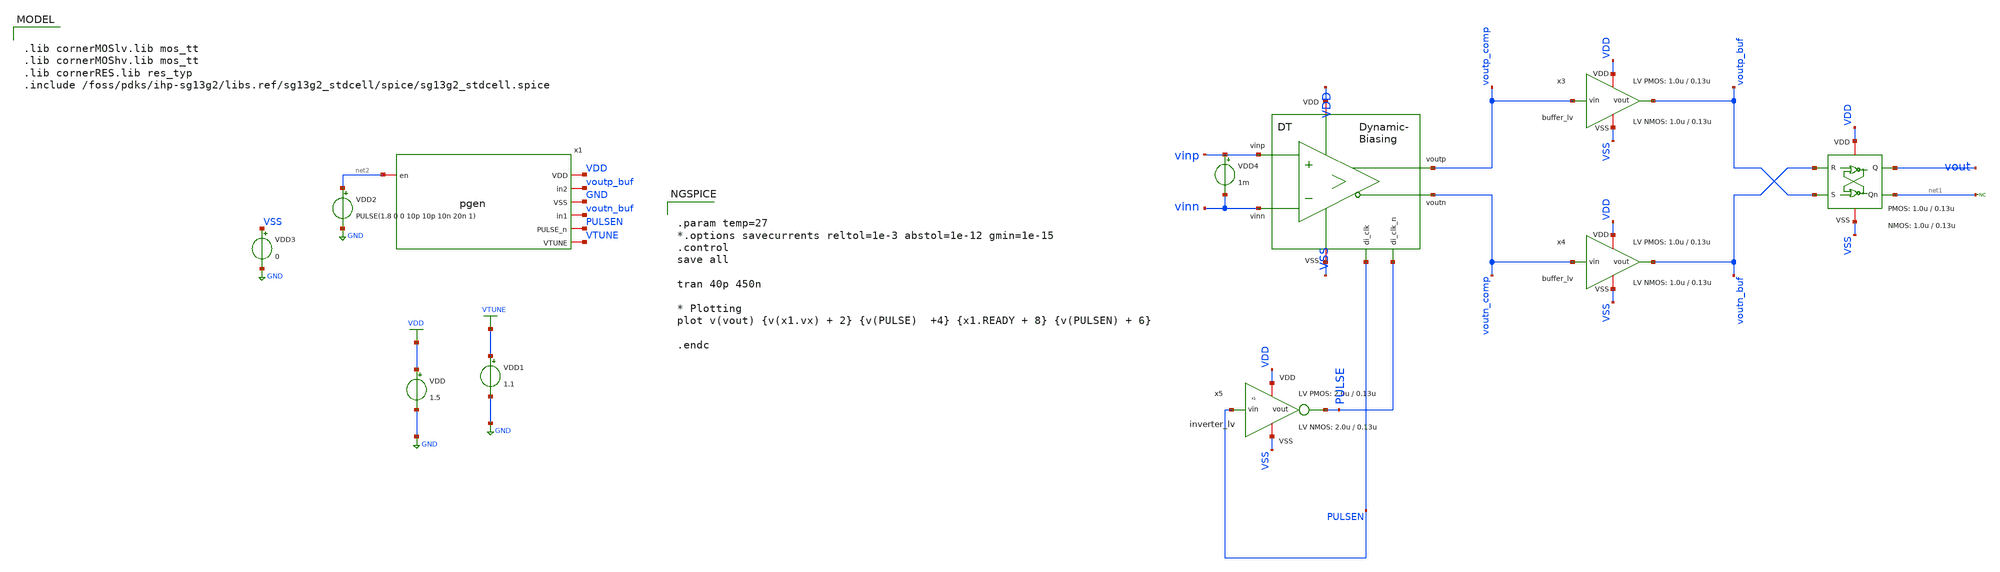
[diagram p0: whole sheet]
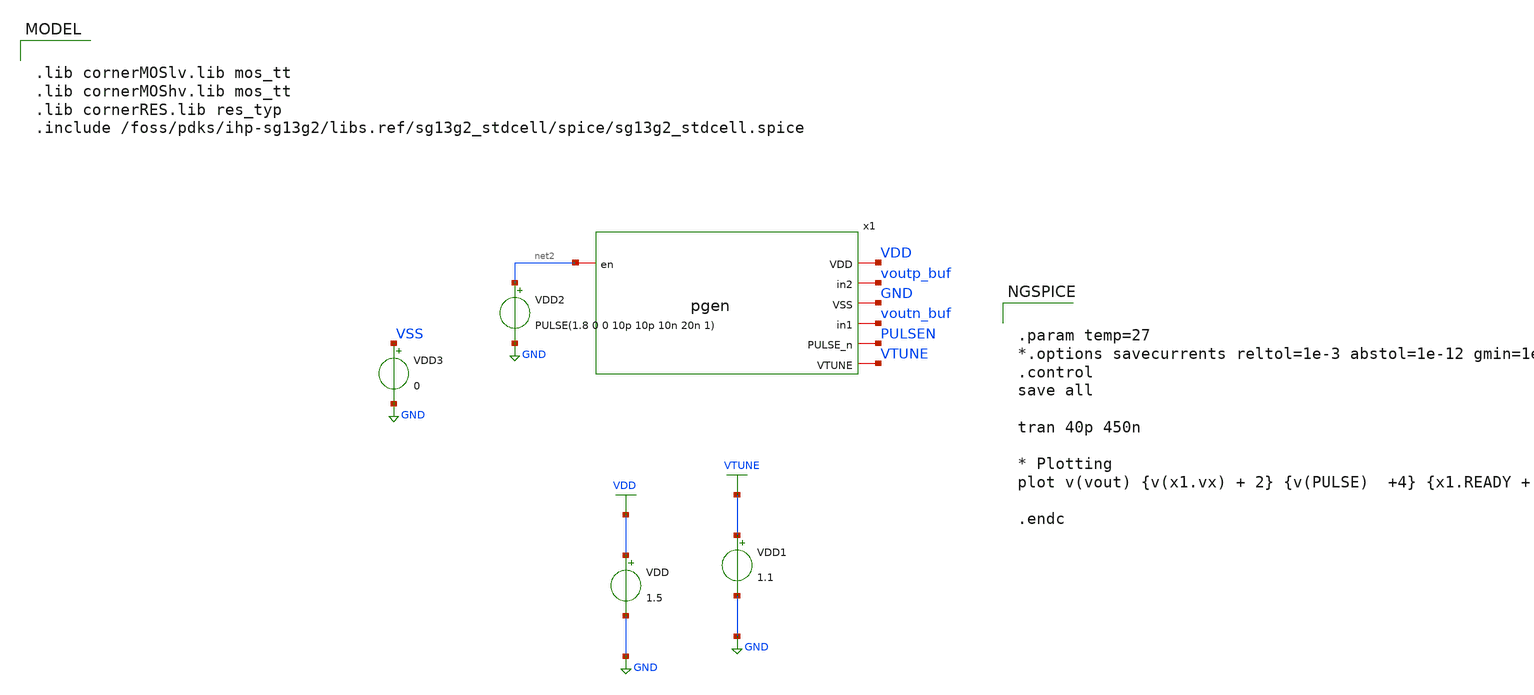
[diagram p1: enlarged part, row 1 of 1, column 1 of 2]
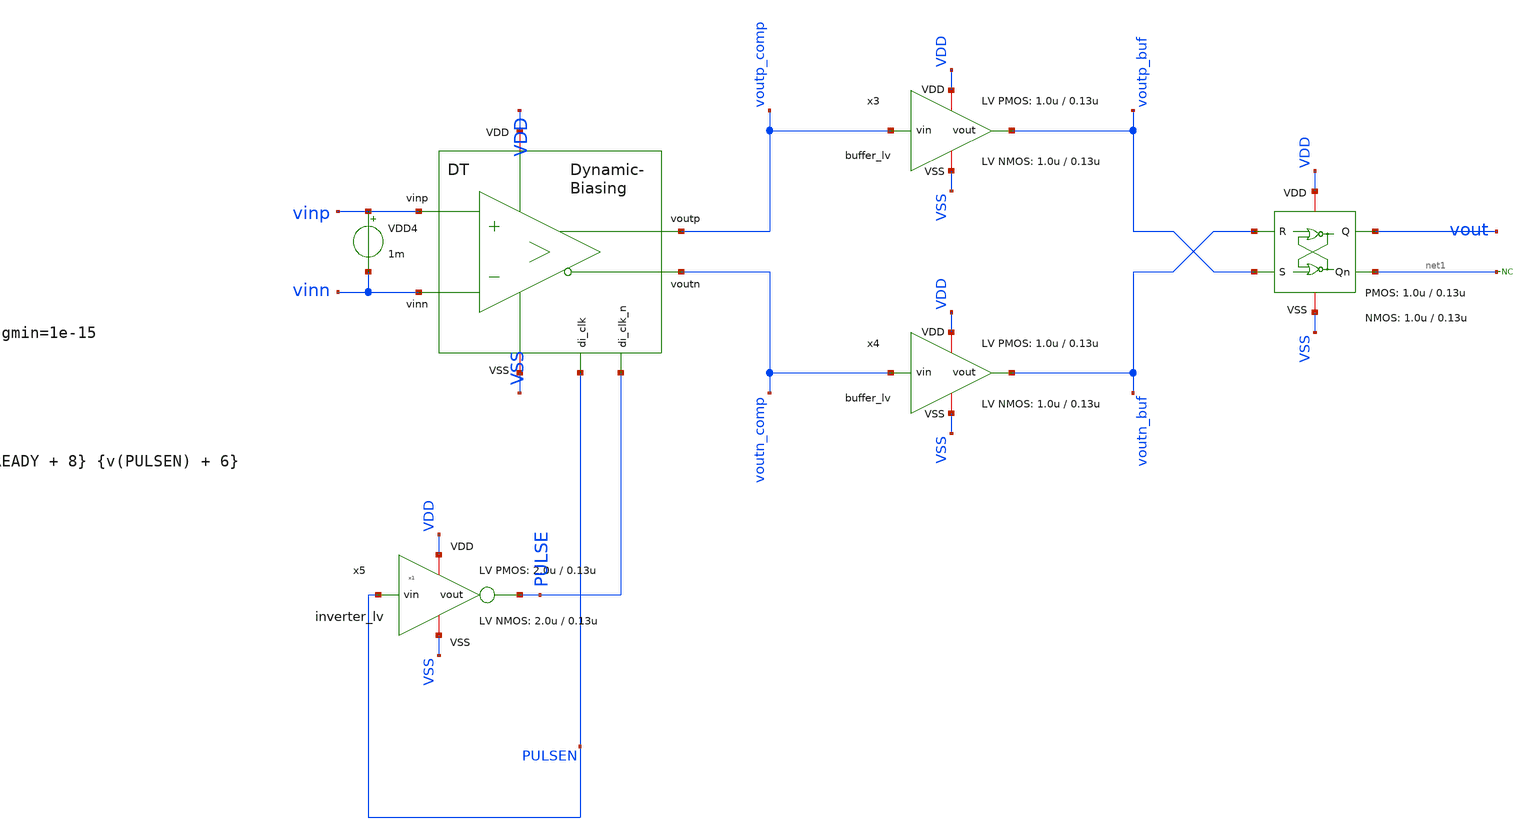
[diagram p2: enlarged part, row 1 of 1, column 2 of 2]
** sch_path: xschem/comparator/pulse_gen/testbench/tb_pgen_comp.sch
**.subckt tb_pgen_comp
x1 VDD voutp_buf GND voutn_buf PULSEN VTUNE net2 pgen
VDD VDD GND 1.5
VDD1 VTUNE GND 1.1
VDD3 VSS GND 0
x5 VDD PULSEN PULSE VSS inverter_lv W_P=2.0u L_P=0.13u W_N=2.0u L_N=0.13u N_C=1
x2 PULSE PULSEN VDD voutp_comp vinp VSS voutn_comp vinn dynamic_biasing_comparator
x3 VDD voutp_comp voutp_buf VSS buffer_lv W_P_INV=1.0u L_P_INV=0.13u W_N_INV=1.0u L_N_INV=0.13u
x4 VDD voutn_comp voutn_buf VSS buffer_lv W_P_INV=1.0u L_P_INV=0.13u W_N_INV=1.0u L_N_INV=0.13u
* noconn #net1
x7 VDD voutp_buf net1 VSS vout voutn_buf SR_latch W_P_SR=1.0u L_P_SR=0.13u W_N_SR=1.0u L_N_SR=0.13u
VDD2 net2 GND PULSE(1.8 0 0 10p 10p 10n 20n 1)
VDD4 vinp vinn 1m
**** begin user architecture code

.lib cornerMOSlv.lib mos_tt
.lib cornerMOShv.lib mos_tt
.lib cornerRES.lib res_typ
.include /foss/pdks/ihp-sg13g2/libs.ref/sg13g2_stdcell/spice/sg13g2_stdcell.spice



.param temp=27
*.options savecurrents reltol=1e-3 abstol=1e-12 gmin=1e-15
.control
save all

tran 40p 450n

* Plotting
plot v(vout) {v(x1.vx) + 2} {v(PULSE)  +4} {x1.READY + 8} {v(PULSEN) + 6}

.endc

**** end user architecture code
**.ends
.GLOBAL GND
.GLOBAL VDD
.GLOBAL VTUNE
.end
